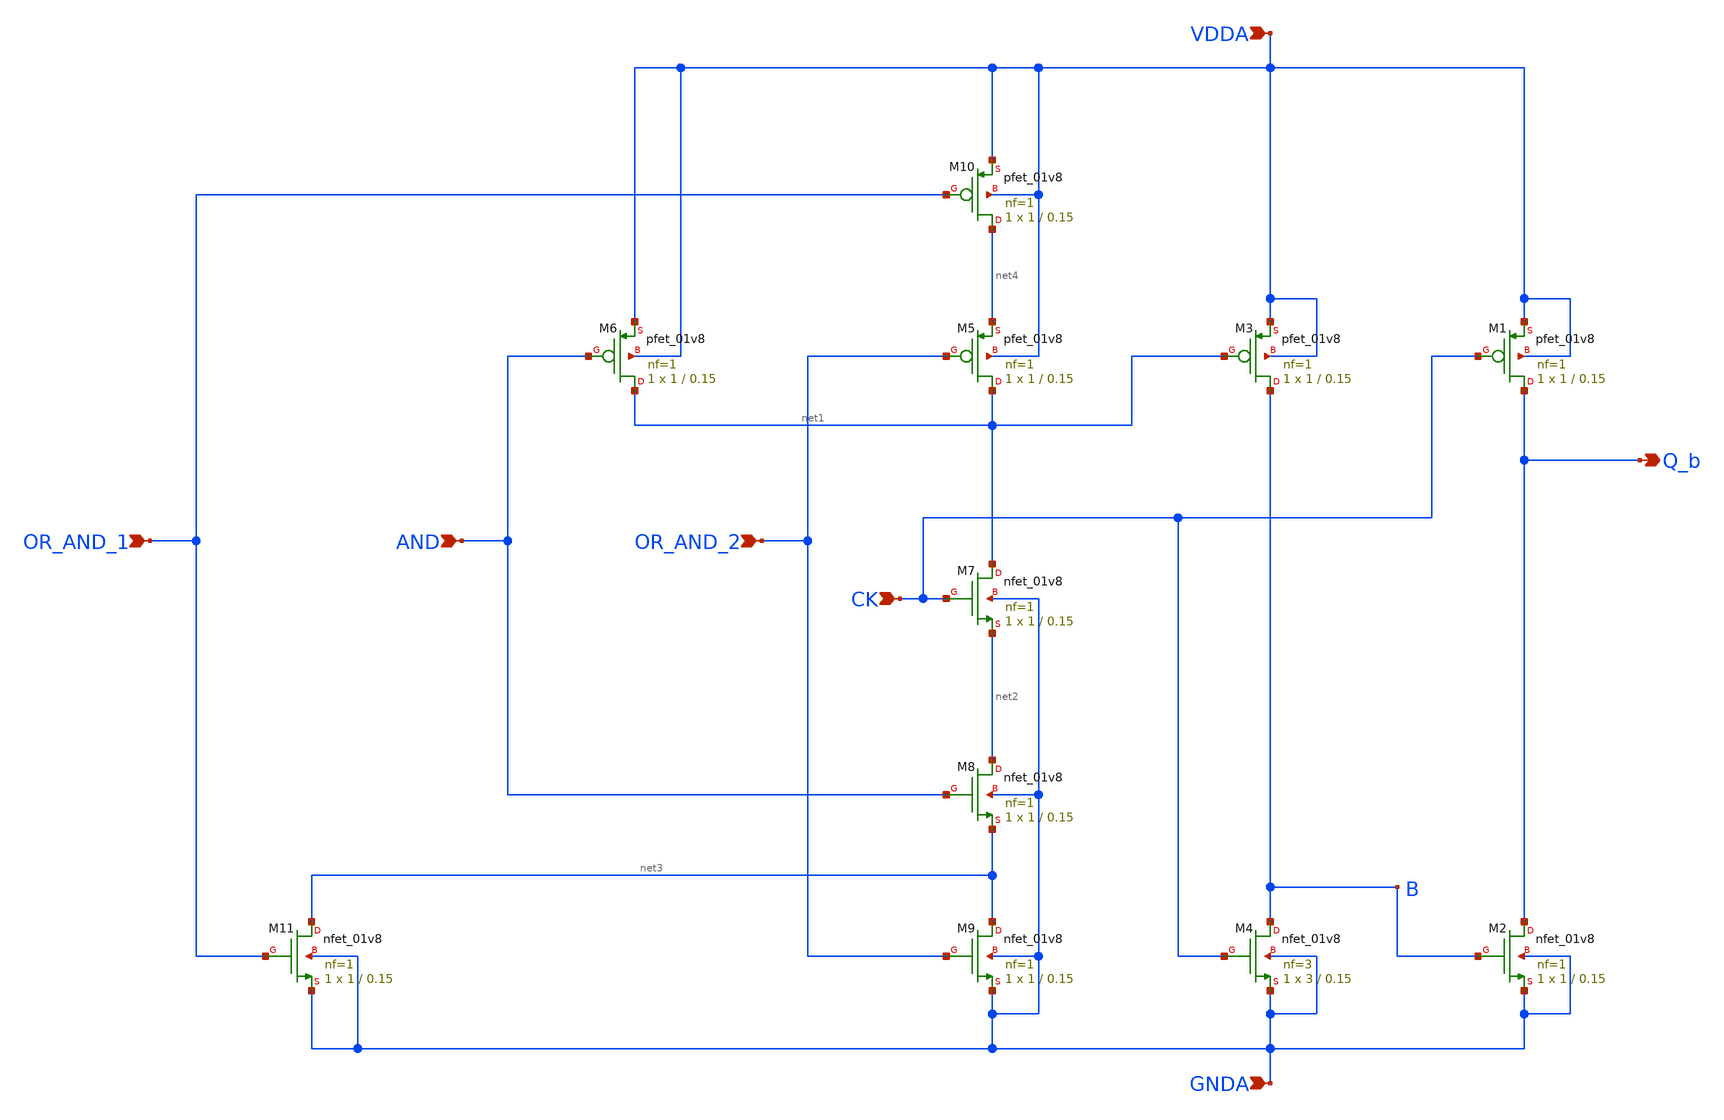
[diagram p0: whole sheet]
** sch_path: projects/pll/divider/xschem_ngspice/TSPC_FF_ratioed_or_and.sch
**.subckt TSPC_FF_ratioed_or_and CK OR_AND_1 Q_b VDDA GNDA AND OR_AND_2
*.ipin CK
*.ipin OR_AND_1
*.opin Q_b
*.ipin VDDA
*.ipin GNDA
*.ipin AND
*.ipin OR_AND_2
XM1 Q_b CK VDDA VDDA sky130_fd_pr__pfet_01v8 L=0.15 W=1 nf=1 ad='int((nf+1)/2) * W/nf * 0.29' as='int((nf+2)/2) * W/nf * 0.29'
+ pd='2*int((nf+1)/2) * (W/nf + 0.29)' ps='2*int((nf+2)/2) * (W/nf + 0.29)' nrd='0.29 / W' nrs='0.29 / W'
+ sa=0 sb=0 sd=0 mult=1 m=1
XM2 Q_b B GNDA GNDA sky130_fd_pr__nfet_01v8 L=0.15 W=1 nf=1 ad='int((nf+1)/2) * W/nf * 0.29' as='int((nf+2)/2) * W/nf * 0.29'
+ pd='2*int((nf+1)/2) * (W/nf + 0.29)' ps='2*int((nf+2)/2) * (W/nf + 0.29)' nrd='0.29 / W' nrs='0.29 / W'
+ sa=0 sb=0 sd=0 mult=1 m=1
XM3 B net1 VDDA VDDA sky130_fd_pr__pfet_01v8 L=0.15 W=1 nf=1 ad='int((nf+1)/2) * W/nf * 0.29' as='int((nf+2)/2) * W/nf * 0.29'
+ pd='2*int((nf+1)/2) * (W/nf + 0.29)' ps='2*int((nf+2)/2) * (W/nf + 0.29)' nrd='0.29 / W' nrs='0.29 / W'
+ sa=0 sb=0 sd=0 mult=1 m=1
XM4 B CK GNDA GNDA sky130_fd_pr__nfet_01v8 L=0.15 W=3 nf=3 ad='int((nf+1)/2) * W/nf * 0.29' as='int((nf+2)/2) * W/nf * 0.29'
+ pd='2*int((nf+1)/2) * (W/nf + 0.29)' ps='2*int((nf+2)/2) * (W/nf + 0.29)' nrd='0.29 / W' nrs='0.29 / W'
+ sa=0 sb=0 sd=0 mult=1 m=1
XM5 net1 OR_AND_2 net4 VDDA sky130_fd_pr__pfet_01v8 L=0.15 W=1 nf=1 ad='int((nf+1)/2) * W/nf * 0.29'
+ as='int((nf+2)/2) * W/nf * 0.29' pd='2*int((nf+1)/2) * (W/nf + 0.29)' ps='2*int((nf+2)/2) * (W/nf + 0.29)'
+ nrd='0.29 / W' nrs='0.29 / W' sa=0 sb=0 sd=0 mult=1 m=1
XM9 net3 OR_AND_2 GNDA GNDA sky130_fd_pr__nfet_01v8 L=0.15 W=1 nf=1 ad='int((nf+1)/2) * W/nf * 0.29'
+ as='int((nf+2)/2) * W/nf * 0.29' pd='2*int((nf+1)/2) * (W/nf + 0.29)' ps='2*int((nf+2)/2) * (W/nf + 0.29)'
+ nrd='0.29 / W' nrs='0.29 / W' sa=0 sb=0 sd=0 mult=1 m=1
XM7 net1 CK net2 GNDA sky130_fd_pr__nfet_01v8 L=0.15 W=1 nf=1 ad='int((nf+1)/2) * W/nf * 0.29' as='int((nf+2)/2) * W/nf * 0.29'
+ pd='2*int((nf+1)/2) * (W/nf + 0.29)' ps='2*int((nf+2)/2) * (W/nf + 0.29)' nrd='0.29 / W' nrs='0.29 / W'
+ sa=0 sb=0 sd=0 mult=1 m=1
XM6 net1 AND VDDA VDDA sky130_fd_pr__pfet_01v8 L=0.15 W=1 nf=1 ad='int((nf+1)/2) * W/nf * 0.29' as='int((nf+2)/2) * W/nf * 0.29'
+ pd='2*int((nf+1)/2) * (W/nf + 0.29)' ps='2*int((nf+2)/2) * (W/nf + 0.29)' nrd='0.29 / W' nrs='0.29 / W'
+ sa=0 sb=0 sd=0 mult=1 m=1
XM8 net2 AND net3 GNDA sky130_fd_pr__nfet_01v8 L=0.15 W=1 nf=1 ad='int((nf+1)/2) * W/nf * 0.29' as='int((nf+2)/2) * W/nf * 0.29'
+ pd='2*int((nf+1)/2) * (W/nf + 0.29)' ps='2*int((nf+2)/2) * (W/nf + 0.29)' nrd='0.29 / W' nrs='0.29 / W'
+ sa=0 sb=0 sd=0 mult=1 m=1
XM10 net4 OR_AND_1 VDDA VDDA sky130_fd_pr__pfet_01v8 L=0.15 W=1 nf=1 ad='int((nf+1)/2) * W/nf * 0.29'
+ as='int((nf+2)/2) * W/nf * 0.29' pd='2*int((nf+1)/2) * (W/nf + 0.29)' ps='2*int((nf+2)/2) * (W/nf + 0.29)'
+ nrd='0.29 / W' nrs='0.29 / W' sa=0 sb=0 sd=0 mult=1 m=1
XM11 net3 OR_AND_1 GNDA GNDA sky130_fd_pr__nfet_01v8 L=0.15 W=1 nf=1 ad='int((nf+1)/2) * W/nf * 0.29'
+ as='int((nf+2)/2) * W/nf * 0.29' pd='2*int((nf+1)/2) * (W/nf + 0.29)' ps='2*int((nf+2)/2) * (W/nf + 0.29)'
+ nrd='0.29 / W' nrs='0.29 / W' sa=0 sb=0 sd=0 mult=1 m=1
**.ends
.end
